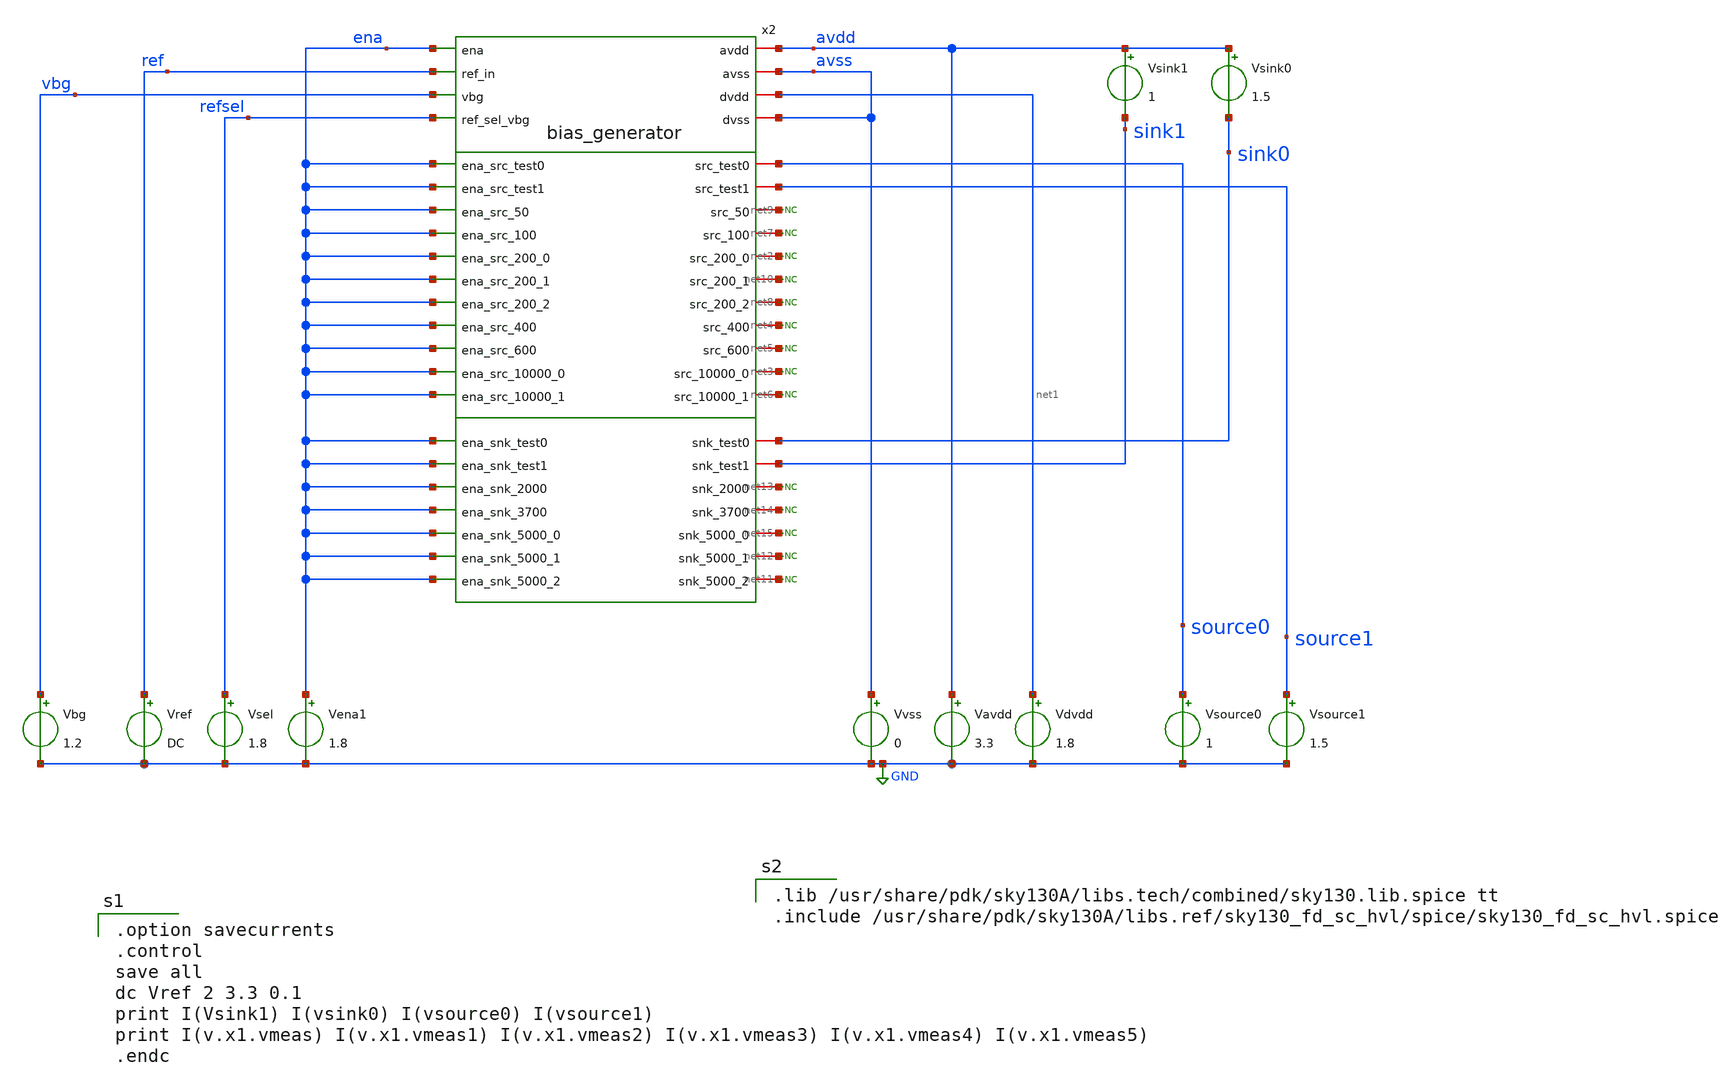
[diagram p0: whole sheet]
** sch_path: xschem/bias_generator_tb.sch
**.subckt bias_generator_tb
Vavdd avdd GND 3.3
Vvss avss GND 0
Vsource0 source0 GND 1
Vsource1 source1 GND 1.5
Vsink1 avdd sink1 1
Vsink0 avdd sink0 1.5
Vsel refsel GND 1.8
Vref ref GND DC
x2 avdd ena ena vbg ena ena ena ena net2 ena net3 net4 net5 source0 source1 net6 net7 net8 net9
+ net10 ena ena ena sink1 net11 net12 net13 net14 sink0 net15 ena ena ena ena ena avss ena net1 ena ena ena
+ refsel ref avss bias_generator
Vbg vbg GND 1.2
Vena1 ena GND 1.8
Vdvdd net1 GND 1.8
* noconn #net9
* noconn #net7
* noconn #net2
* noconn #net10
* noconn #net8
* noconn #net4
* noconn #net5
* noconn #net3
* noconn #net6
* noconn #net13
* noconn #net14
* noconn #net15
* noconn #net12
* noconn #net11
**** begin user architecture code

.option savecurrents
.control
save all
dc Vref 2 3.3 0.1
print I(Vsink1) I(vsink0) I(vsource0) I(vsource1)
print I(v.x1.vmeas) I(v.x1.vmeas1) I(v.x1.vmeas2) I(v.x1.vmeas3) I(v.x1.vmeas4) I(v.x1.vmeas5)
.endc


.lib /usr/share/pdk/sky130A/libs.tech/combined/sky130.lib.spice tt
.include /usr/share/pdk/sky130A/libs.ref/sky130_fd_sc_hvl/spice/sky130_fd_sc_hvl.spice


**** end user architecture code
**.ends
.GLOBAL GND
.end
